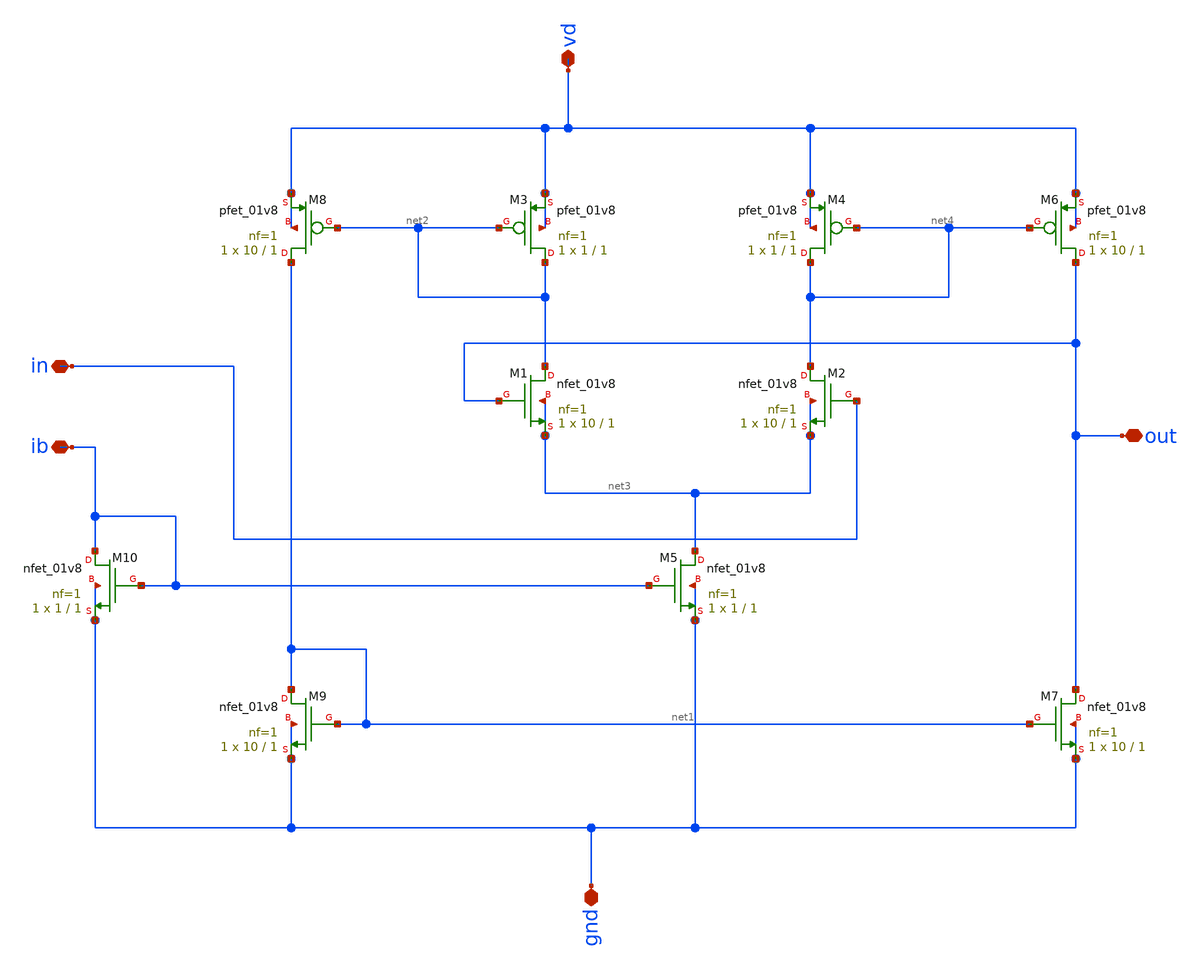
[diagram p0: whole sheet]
** sch_path: buffer/xschem/buffer.sch
* Copyright 2020 Stefan Frederik Schippers
* Licensed under the Apache License, Version 2.0 (the "License");
* you may not use this file except in compliance with the License.
* You may obtain a copy of the License at
* https://www.apache.org/licenses/LICENSE-2.0
* Unless required by applicable law or agreed to in writing, software
* distributed under the License is distributed on an "AS IS" BASIS,
* WITHOUT WARRANTIES OR CONDITIONS OF ANY KIND, either express or implied.
* See the License for the specific language governing permissions and
* limitations under the License.
**.subckt buffer vd ib out in gnd
*.iopin vd
*.iopin ib
*.iopin out
*.iopin in
*.iopin gnd
XM3 net2 net2 vd vd sky130_fd_pr__pfet_01v8 L=1 W=1 nf=1 ad='int((nf+1)/2) * W/nf * 0.29' as='int((nf+2)/2) * W/nf * 0.29'
+ pd='2*int((nf+1)/2) * (W/nf + 0.29)' ps='2*int((nf+2)/2) * (W/nf + 0.29)' nrd='0.29 / W' nrs='0.29 / W'
+ sa=0 sb=0 sd=0 mult=1 m=1
XM1 net2 out net3 net3 sky130_fd_pr__nfet_01v8 L=1 W=10 nf=1 ad='int((nf+1)/2) * W/nf * 0.29' as='int((nf+2)/2) * W/nf * 0.29'
+ pd='2*int((nf+1)/2) * (W/nf + 0.29)' ps='2*int((nf+2)/2) * (W/nf + 0.29)' nrd='0.29 / W' nrs='0.29 / W'
+ sa=0 sb=0 sd=0 mult=1 m=1
XM2 net4 in net3 net3 sky130_fd_pr__nfet_01v8 L=1 W=10 nf=1 ad='int((nf+1)/2) * W/nf * 0.29' as='int((nf+2)/2) * W/nf * 0.29'
+ pd='2*int((nf+1)/2) * (W/nf + 0.29)' ps='2*int((nf+2)/2) * (W/nf + 0.29)' nrd='0.29 / W' nrs='0.29 / W'
+ sa=0 sb=0 sd=0 mult=1 m=1
XM4 net4 net4 vd vd sky130_fd_pr__pfet_01v8 L=1 W=1 nf=1 ad='int((nf+1)/2) * W/nf * 0.29' as='int((nf+2)/2) * W/nf * 0.29'
+ pd='2*int((nf+1)/2) * (W/nf + 0.29)' ps='2*int((nf+2)/2) * (W/nf + 0.29)' nrd='0.29 / W' nrs='0.29 / W'
+ sa=0 sb=0 sd=0 mult=1 m=1
XM5 net3 ib gnd gnd sky130_fd_pr__nfet_01v8 L=1 W=1 nf=1 ad='int((nf+1)/2) * W/nf * 0.29' as='int((nf+2)/2) * W/nf * 0.29'
+ pd='2*int((nf+1)/2) * (W/nf + 0.29)' ps='2*int((nf+2)/2) * (W/nf + 0.29)' nrd='0.29 / W' nrs='0.29 / W'
+ sa=0 sb=0 sd=0 mult=1 m=1
XM6 out net4 vd vd sky130_fd_pr__pfet_01v8 L=1 W=10 nf=1 ad='int((nf+1)/2) * W/nf * 0.29' as='int((nf+2)/2) * W/nf * 0.29'
+ pd='2*int((nf+1)/2) * (W/nf + 0.29)' ps='2*int((nf+2)/2) * (W/nf + 0.29)' nrd='0.29 / W' nrs='0.29 / W'
+ sa=0 sb=0 sd=0 mult=1 m=1
XM7 out net1 gnd gnd sky130_fd_pr__nfet_01v8 L=1 W=10 nf=1 ad='int((nf+1)/2) * W/nf * 0.29' as='int((nf+2)/2) * W/nf * 0.29'
+ pd='2*int((nf+1)/2) * (W/nf + 0.29)' ps='2*int((nf+2)/2) * (W/nf + 0.29)' nrd='0.29 / W' nrs='0.29 / W'
+ sa=0 sb=0 sd=0 mult=1 m=1
XM8 net1 net2 vd vd sky130_fd_pr__pfet_01v8 L=1 W=10 nf=1 ad='int((nf+1)/2) * W/nf * 0.29' as='int((nf+2)/2) * W/nf * 0.29'
+ pd='2*int((nf+1)/2) * (W/nf + 0.29)' ps='2*int((nf+2)/2) * (W/nf + 0.29)' nrd='0.29 / W' nrs='0.29 / W'
+ sa=0 sb=0 sd=0 mult=1 m=1
XM9 net1 net1 gnd gnd sky130_fd_pr__nfet_01v8 L=1 W=10 nf=1 ad='int((nf+1)/2) * W/nf * 0.29' as='int((nf+2)/2) * W/nf * 0.29'
+ pd='2*int((nf+1)/2) * (W/nf + 0.29)' ps='2*int((nf+2)/2) * (W/nf + 0.29)' nrd='0.29 / W' nrs='0.29 / W'
+ sa=0 sb=0 sd=0 mult=1 m=1
XM10 ib ib gnd gnd sky130_fd_pr__nfet_01v8 L=1 W=1 nf=1 ad='int((nf+1)/2) * W/nf * 0.29' as='int((nf+2)/2) * W/nf * 0.29'
+ pd='2*int((nf+1)/2) * (W/nf + 0.29)' ps='2*int((nf+2)/2) * (W/nf + 0.29)' nrd='0.29 / W' nrs='0.29 / W'
+ sa=0 sb=0 sd=0 mult=1 m=1
**** begin user architecture code




**** end user architecture code
**.ends
.end
